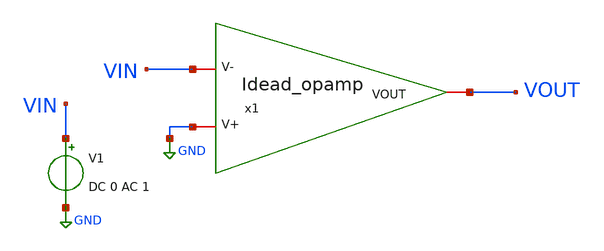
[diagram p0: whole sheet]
** sch_path: Design/Testbench_OL.sch
**.subckt Testbench_OL
x1 VOUT VIN GND Idead_opamp
V1 VIN GND DC 0 AC 1
**** begin user architecture code


.include sim_script_OL.sim


**** end user architecture code
**.ends

* expanding   symbol:  Idead_opamp.sym # of pins=3
** sym_path: Design/Idead_opamp.sym
** sch_path: Design/Idead_opamp.sch
.subckt Idead_opamp VOUT V- V+
*.iopin V-
*.iopin V+
*.iopin VOUT
E1 VOUT1 GND V+ V- 10000
B1 VOUT GND V = max(-1, min(1, V(VOUT1)))
.ends

.GLOBAL GND
.end
